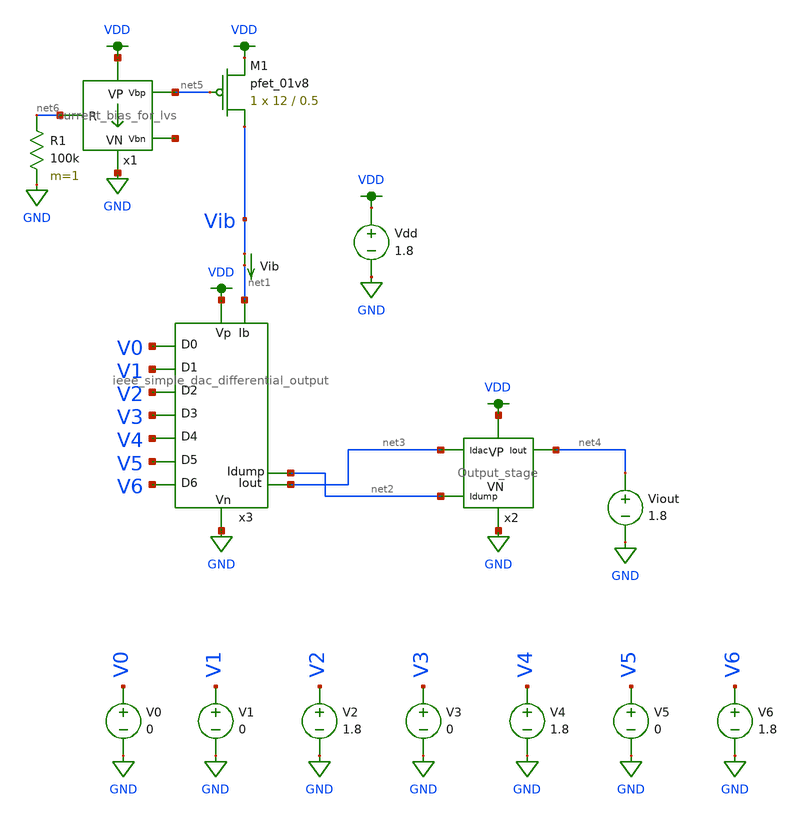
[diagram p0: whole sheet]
** sch_path: schematics/ieee DAC/ieee_DAC_mc_simulation_12.sch
**.subckt ieee_DAC_mc_simulation_12
Vdd VDD GND 1.8
V1 V1 GND 0
V2 V2 GND 1.8
V3 V3 GND 0
V4 V4 GND 1.8
V5 V5 GND 0
V6 V6 GND 1.8
V0 V0 GND 0
Vib Vib net1 0
.save i(vib)
x2 VDD GND net4 net3 net2 Output_stage
x3 VDD net2 GND V1 V0 V2 V3 V4 V5 V6 net1 net3 ieee_simple_dac_differential_output
Viout net4 GND 1.8
x1 VDD GND net5 net7 net6 current_bias_for_lvs
XM1 Vib net5 VDD VDD sky130_fd_pr__pfet_01v8 L=0.5 W=12 nf=1 ad='int((nf+1)/2) * W/nf * 0.29' as='int((nf+2)/2) * W/nf * 0.29'
+ pd='2*int((nf+1)/2) * (W/nf + 0.29)' ps='2*int((nf+2)/2) * (W/nf + 0.29)' nrd='0.29 / W' nrs='0.29 / W'
+ sa=0 sb=0 sd=0 mult=1 m=1
R1 net6 GND 100k m=1
**** begin user architecture code

.option wnflag=1
.param MC_SWITCH=0.0
.lib ~/skywater/skywater-pdk/libraries/sky130_fd_pr_ngspice/latest/models/sky130.lib.spice tt


.save all
.control
set wr_vecnames
set wr_singlescale

let Ibias_max = 31n
let Ibias = 30n
dowhile Ibias < Ibias_max
alter Ib $&Ibias

let mc_runs = 1
let run = 1
dowhile run <= mc_runs

  let code = 0
  while code < 128
    if floor(code / 1) eq 0
      let b0 = 0
    else
      let b0 = (floor(code / 1) % 2) * 1.8
    end
    if floor(code / 2) eq 0
      let b1 = 0
    else
      let b1 = (floor(code / 2) % 2) * 1.8
    end
    if floor(code / 4) eq 0
      let b2 = 0
    else
      let b2 = (floor(code / 4) % 2) * 1.8
    end
    if floor(code / 8) eq 0
      let b3 = 0
    else
      let b3 = (floor(code / 8) % 2) * 1.8
    end
    if floor(code / 16) eq 0
      let b4 = 0
    else
      let b4 = (floor(code / 16) % 2) * 1.8
    end
    if floor(code / 32) eq 0
      let b5 = 0
    else
      let b5 = (floor(code / 32) % 2) * 1.8
    end
    if floor(code / 64) eq 0
      let b6 = 0
    else
      let b6 = (floor(code / 64) % 2) * 1.8
    end

    alter V0 $&b0
    alter V1 $&b1
    alter V2 $&b2
    alter V3 $&b3
    alter V4 $&b4
    alter V5 $&b5
    alter V6 $&b6
    save all
    op

    wrdata ~/dev/git/7-bit-D-A-converter-MP4-MADVLSI/schematics/simulations/ieee_DAC/dac_with_external_bias_gen/test_16/ieeeDAC_{$&run}.txt
+ V0 V1 V2 V3 V4 V5 V6 i(Vib) i(Viout)
    if code eq 0
      set appendwrite
      set wr_vecnames = FALSE
    end
    let code = code + 1
  end
  reset
  set appendwrite = FALSE
  set wr_vecnames
  let run = run + 1
end

let Ibias = Ibias * 2
end
.endc

**** end user architecture code
**.ends
.GLOBAL VDD
.GLOBAL GND
.end
